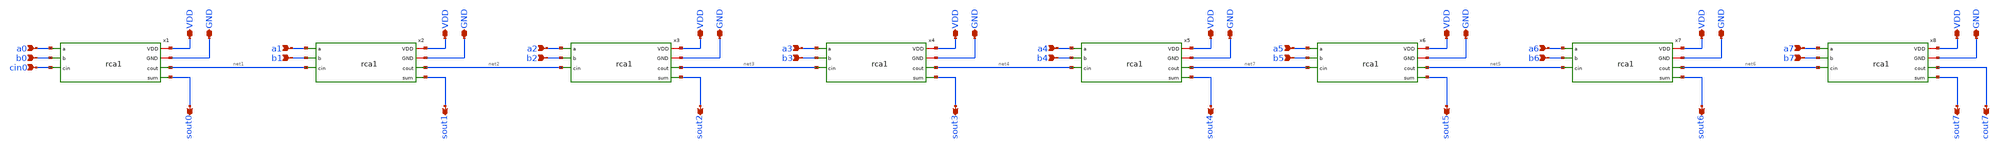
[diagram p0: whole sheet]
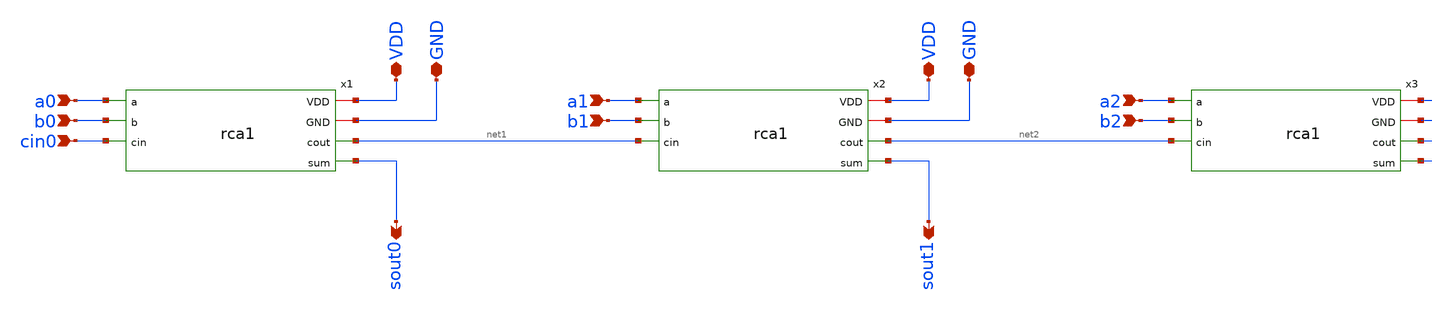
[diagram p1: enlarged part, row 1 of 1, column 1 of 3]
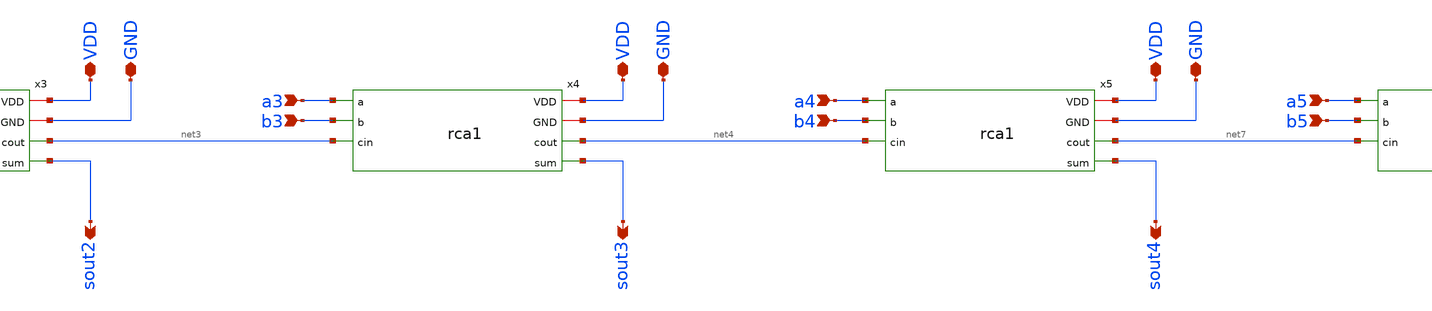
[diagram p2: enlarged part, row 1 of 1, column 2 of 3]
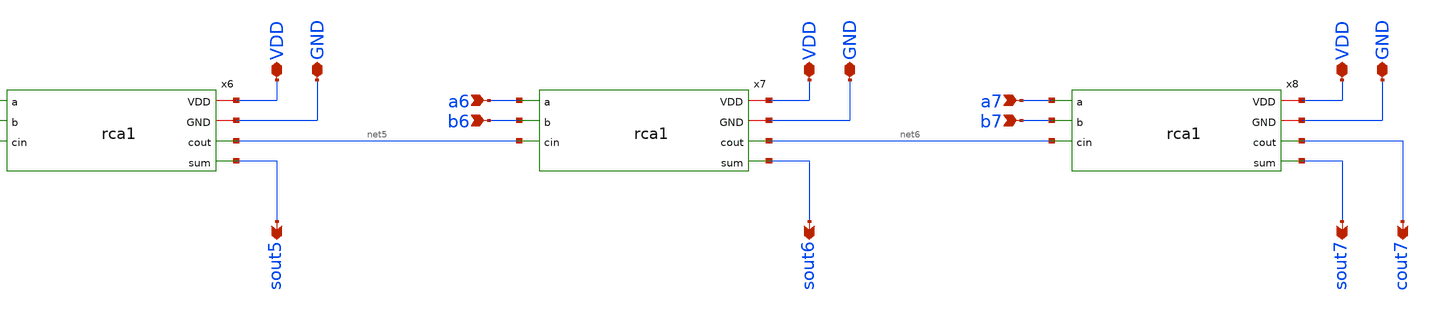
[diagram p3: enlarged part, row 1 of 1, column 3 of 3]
** sch_path: assignments/assignment8/rca8.sch
**.subckt rca8 a0 b0 cin0 sout0 VDD GND a1 b1 sout1 VDD GND a2 b2 sout2 VDD GND a3 b3 sout3 VDD GND
*+ a4 b4 sout4 VDD GND a5 b5 sout5 VDD GND a6 b6 sout6 VDD GND a7 b7 sout7 VDD GND cout7
*.ipin a0
*.ipin b0
*.ipin cin0
*.opin sout0
*.iopin VDD
*.iopin GND
*.ipin a1
*.ipin b1
*.opin sout1
*.iopin VDD
*.iopin GND
*.ipin a2
*.ipin b2
*.opin sout2
*.iopin VDD
*.iopin GND
*.ipin a3
*.ipin b3
*.opin sout3
*.iopin VDD
*.iopin GND
*.ipin a4
*.ipin b4
*.opin sout4
*.iopin VDD
*.iopin GND
*.ipin a5
*.ipin b5
*.opin sout5
*.iopin VDD
*.iopin GND
*.ipin a6
*.ipin b6
*.opin sout6
*.iopin VDD
*.iopin GND
*.ipin a7
*.ipin b7
*.opin sout7
*.iopin VDD
*.iopin GND
*.opin cout7
x1 VDD a0 b0 cin0 GND net1 sout0 rca1
x2 VDD a1 b1 net1 GND net2 sout1 rca1
x3 VDD a2 b2 net2 GND net3 sout2 rca1
x4 VDD a3 b3 net3 GND net4 sout3 rca1
x5 VDD a4 b4 net4 GND net7 sout4 rca1
x6 VDD a5 b5 net7 GND net5 sout5 rca1
x7 VDD a6 b6 net5 GND net6 sout6 rca1
x8 VDD a7 b7 net6 GND cout7 sout7 rca1
**.ends
.end
